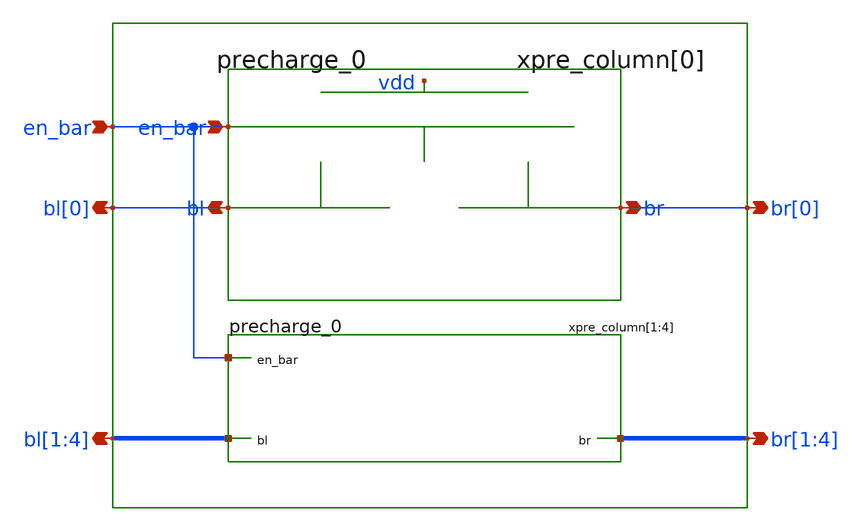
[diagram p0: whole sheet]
** sch_path: sram_4_16_scn4m/precharge_array.sch
**.subckt precharge_array bl[0] br[0] en_bar bl[1],bl[2],bl[3],bl[4] br[1],br[2],br[3],br[4]
*.opin bl[0]
*.opin br[0]
*.ipin en_bar
*.opin bl[1],bl[2],bl[3],bl[4]
*.opin br[1],br[2],br[3],br[4]
xpre_column[0] bl[0] br[0] en_bar vdd precharge_0
xpre_column[1] bl[1] br[1] en_bar vdd precharge_0
xpre_column[2] bl[2] br[2] en_bar vdd precharge_0
xpre_column[3] bl[3] br[3] en_bar vdd precharge_0
xpre_column[4] bl[4] br[4] en_bar vdd precharge_0
**.ends

* expanding   symbol:  precharge_0.sch # of pins=3
** sym_path: sram_4_16_scn4m/precharge_0.sch
** sch_path: sram_4_16_scn4m/precharge_0.sch
.subckt precharge_0 bl br en_bar vdd
*.opin bl
*.opin br
*.ipin en_bar
XMupper_pmos1 bl en_bar vdd vdd sky130_fd_pr__pfet_01v8 L=0.4 W=1.6 nf=1 ad='int((nf+1)/2) * W/nf * 0.29'
+ as='int((nf+2)/2) * W/nf * 0.29' pd='2*int((nf+1)/2) * (W/nf + 0.29)' ps='2*int((nf+2)/2) * (W/nf + 0.29)'
+ nrd='0.29 / W' nrs='0.29 / W' sa=0 sb=0 sd=0 mult=1 m=1
XMupper_pmos2 br en_bar vdd vdd sky130_fd_pr__pfet_01v8 L=0.4 W=1.6 nf=1 ad='int((nf+1)/2) * W/nf * 0.29'
+ as='int((nf+2)/2) * W/nf * 0.29' pd='2*int((nf+1)/2) * (W/nf + 0.29)' ps='2*int((nf+2)/2) * (W/nf + 0.29)'
+ nrd='0.29 / W' nrs='0.29 / W' sa=0 sb=0 sd=0 mult=1 m=1
XMlower_pmos br en_bar bl vdd sky130_fd_pr__pfet_01v8 L=0.4 W=1.6 nf=1 ad='int((nf+1)/2) * W/nf * 0.29'
+ as='int((nf+2)/2) * W/nf * 0.29' pd='2*int((nf+1)/2) * (W/nf + 0.29)' ps='2*int((nf+2)/2) * (W/nf + 0.29)'
+ nrd='0.29 / W' nrs='0.29 / W' sa=0 sb=0 sd=0 mult=1 m=1
.ends

.end
